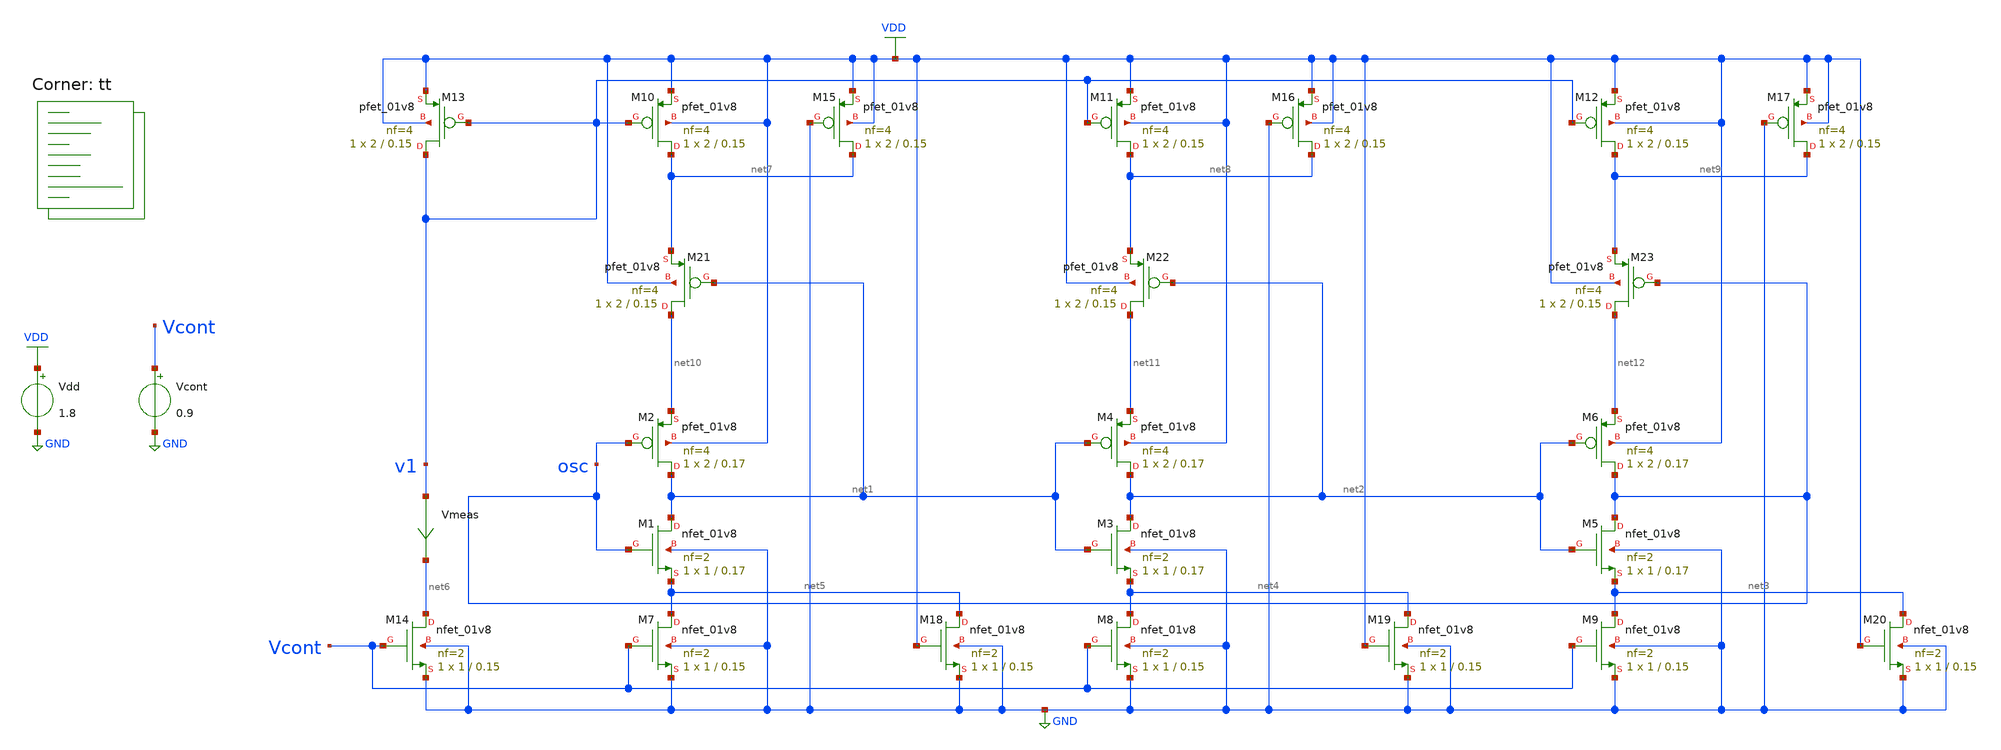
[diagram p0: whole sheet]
** sch_path: projects/pll/vco/xschem_ngspice/tb_current_starved_VCO2.sch
**.subckt tb_current_starved_VCO2
XM1 net1 osc net5 GND sky130_fd_pr__nfet_01v8 L=0.17 W=1 nf=2 ad='int((nf+1)/2) * W/nf * 0.29' as='int((nf+2)/2) * W/nf * 0.29'
+ pd='2*int((nf+1)/2) * (W/nf + 0.29)' ps='2*int((nf+2)/2) * (W/nf + 0.29)' nrd='0.29 / W' nrs='0.29 / W'
+ sa=0 sb=0 sd=0 mult=1 m=1
XM2 net1 osc net10 VDD sky130_fd_pr__pfet_01v8 L=0.17 W=2 nf=4 ad='int((nf+1)/2) * W/nf * 0.29' as='int((nf+2)/2) * W/nf * 0.29'
+ pd='2*int((nf+1)/2) * (W/nf + 0.29)' ps='2*int((nf+2)/2) * (W/nf + 0.29)' nrd='0.29 / W' nrs='0.29 / W'
+ sa=0 sb=0 sd=0 mult=1 m=1
XM3 net2 net1 net4 GND sky130_fd_pr__nfet_01v8 L=0.17 W=1 nf=2 ad='int((nf+1)/2) * W/nf * 0.29' as='int((nf+2)/2) * W/nf * 0.29'
+ pd='2*int((nf+1)/2) * (W/nf + 0.29)' ps='2*int((nf+2)/2) * (W/nf + 0.29)' nrd='0.29 / W' nrs='0.29 / W'
+ sa=0 sb=0 sd=0 mult=1 m=1
XM4 net2 net1 net11 VDD sky130_fd_pr__pfet_01v8 L=0.17 W=2 nf=4 ad='int((nf+1)/2) * W/nf * 0.29' as='int((nf+2)/2) * W/nf * 0.29'
+ pd='2*int((nf+1)/2) * (W/nf + 0.29)' ps='2*int((nf+2)/2) * (W/nf + 0.29)' nrd='0.29 / W' nrs='0.29 / W'
+ sa=0 sb=0 sd=0 mult=1 m=1
XM5 osc net2 net3 GND sky130_fd_pr__nfet_01v8 L=0.17 W=1 nf=2 ad='int((nf+1)/2) * W/nf * 0.29' as='int((nf+2)/2) * W/nf * 0.29'
+ pd='2*int((nf+1)/2) * (W/nf + 0.29)' ps='2*int((nf+2)/2) * (W/nf + 0.29)' nrd='0.29 / W' nrs='0.29 / W'
+ sa=0 sb=0 sd=0 mult=1 m=1
XM6 osc net2 net12 VDD sky130_fd_pr__pfet_01v8 L=0.17 W=2 nf=4 ad='int((nf+1)/2) * W/nf * 0.29' as='int((nf+2)/2) * W/nf * 0.29'
+ pd='2*int((nf+1)/2) * (W/nf + 0.29)' ps='2*int((nf+2)/2) * (W/nf + 0.29)' nrd='0.29 / W' nrs='0.29 / W'
+ sa=0 sb=0 sd=0 mult=1 m=1
XM7 net5 Vcont GND GND sky130_fd_pr__nfet_01v8 L=0.15 W=1 nf=2 ad='int((nf+1)/2) * W/nf * 0.29' as='int((nf+2)/2) * W/nf * 0.29'
+ pd='2*int((nf+1)/2) * (W/nf + 0.29)' ps='2*int((nf+2)/2) * (W/nf + 0.29)' nrd='0.29 / W' nrs='0.29 / W'
+ sa=0 sb=0 sd=0 mult=1 m=1
XM8 net4 Vcont GND GND sky130_fd_pr__nfet_01v8 L=0.15 W=1 nf=2 ad='int((nf+1)/2) * W/nf * 0.29' as='int((nf+2)/2) * W/nf * 0.29'
+ pd='2*int((nf+1)/2) * (W/nf + 0.29)' ps='2*int((nf+2)/2) * (W/nf + 0.29)' nrd='0.29 / W' nrs='0.29 / W'
+ sa=0 sb=0 sd=0 mult=1 m=1
XM9 net3 Vcont GND GND sky130_fd_pr__nfet_01v8 L=0.15 W=1 nf=2 ad='int((nf+1)/2) * W/nf * 0.29' as='int((nf+2)/2) * W/nf * 0.29'
+ pd='2*int((nf+1)/2) * (W/nf + 0.29)' ps='2*int((nf+2)/2) * (W/nf + 0.29)' nrd='0.29 / W' nrs='0.29 / W'
+ sa=0 sb=0 sd=0 mult=1 m=1
XM10 net7 v1 VDD VDD sky130_fd_pr__pfet_01v8 L=0.15 W=2 nf=4 ad='int((nf+1)/2) * W/nf * 0.29' as='int((nf+2)/2) * W/nf * 0.29'
+ pd='2*int((nf+1)/2) * (W/nf + 0.29)' ps='2*int((nf+2)/2) * (W/nf + 0.29)' nrd='0.29 / W' nrs='0.29 / W'
+ sa=0 sb=0 sd=0 mult=1 m=1
XM11 net8 v1 VDD VDD sky130_fd_pr__pfet_01v8 L=0.15 W=2 nf=4 ad='int((nf+1)/2) * W/nf * 0.29' as='int((nf+2)/2) * W/nf * 0.29'
+ pd='2*int((nf+1)/2) * (W/nf + 0.29)' ps='2*int((nf+2)/2) * (W/nf + 0.29)' nrd='0.29 / W' nrs='0.29 / W'
+ sa=0 sb=0 sd=0 mult=1 m=1
XM12 net9 v1 VDD VDD sky130_fd_pr__pfet_01v8 L=0.15 W=2 nf=4 ad='int((nf+1)/2) * W/nf * 0.29' as='int((nf+2)/2) * W/nf * 0.29'
+ pd='2*int((nf+1)/2) * (W/nf + 0.29)' ps='2*int((nf+2)/2) * (W/nf + 0.29)' nrd='0.29 / W' nrs='0.29 / W'
+ sa=0 sb=0 sd=0 mult=1 m=1
Vdd VDD GND 1.8
Vcont Vcont GND 0.9
XM13 v1 v1 VDD VDD sky130_fd_pr__pfet_01v8 L=0.15 W=2 nf=4 ad='int((nf+1)/2) * W/nf * 0.29' as='int((nf+2)/2) * W/nf * 0.29'
+ pd='2*int((nf+1)/2) * (W/nf + 0.29)' ps='2*int((nf+2)/2) * (W/nf + 0.29)' nrd='0.29 / W' nrs='0.29 / W'
+ sa=0 sb=0 sd=0 mult=1 m=1
XM14 net6 Vcont GND GND sky130_fd_pr__nfet_01v8 L=0.15 W=1 nf=2 ad='int((nf+1)/2) * W/nf * 0.29' as='int((nf+2)/2) * W/nf * 0.29'
+ pd='2*int((nf+1)/2) * (W/nf + 0.29)' ps='2*int((nf+2)/2) * (W/nf + 0.29)' nrd='0.29 / W' nrs='0.29 / W'
+ sa=0 sb=0 sd=0 mult=1 m=1
Vmeas v1 net6 0
.save i(vmeas)
XM15 net7 GND VDD VDD sky130_fd_pr__pfet_01v8 L=0.15 W=2 nf=4 ad='int((nf+1)/2) * W/nf * 0.29' as='int((nf+2)/2) * W/nf * 0.29'
+ pd='2*int((nf+1)/2) * (W/nf + 0.29)' ps='2*int((nf+2)/2) * (W/nf + 0.29)' nrd='0.29 / W' nrs='0.29 / W'
+ sa=0 sb=0 sd=0 mult=1 m=1
XM16 net8 GND VDD VDD sky130_fd_pr__pfet_01v8 L=0.15 W=2 nf=4 ad='int((nf+1)/2) * W/nf * 0.29' as='int((nf+2)/2) * W/nf * 0.29'
+ pd='2*int((nf+1)/2) * (W/nf + 0.29)' ps='2*int((nf+2)/2) * (W/nf + 0.29)' nrd='0.29 / W' nrs='0.29 / W'
+ sa=0 sb=0 sd=0 mult=1 m=1
XM17 net9 GND VDD VDD sky130_fd_pr__pfet_01v8 L=0.15 W=2 nf=4 ad='int((nf+1)/2) * W/nf * 0.29' as='int((nf+2)/2) * W/nf * 0.29'
+ pd='2*int((nf+1)/2) * (W/nf + 0.29)' ps='2*int((nf+2)/2) * (W/nf + 0.29)' nrd='0.29 / W' nrs='0.29 / W'
+ sa=0 sb=0 sd=0 mult=1 m=1
XM18 net5 VDD GND GND sky130_fd_pr__nfet_01v8 L=0.15 W=1 nf=2 ad='int((nf+1)/2) * W/nf * 0.29' as='int((nf+2)/2) * W/nf * 0.29'
+ pd='2*int((nf+1)/2) * (W/nf + 0.29)' ps='2*int((nf+2)/2) * (W/nf + 0.29)' nrd='0.29 / W' nrs='0.29 / W'
+ sa=0 sb=0 sd=0 mult=1 m=1
XM19 net4 VDD GND GND sky130_fd_pr__nfet_01v8 L=0.15 W=1 nf=2 ad='int((nf+1)/2) * W/nf * 0.29' as='int((nf+2)/2) * W/nf * 0.29'
+ pd='2*int((nf+1)/2) * (W/nf + 0.29)' ps='2*int((nf+2)/2) * (W/nf + 0.29)' nrd='0.29 / W' nrs='0.29 / W'
+ sa=0 sb=0 sd=0 mult=1 m=1
XM20 net3 VDD GND GND sky130_fd_pr__nfet_01v8 L=0.15 W=1 nf=2 ad='int((nf+1)/2) * W/nf * 0.29' as='int((nf+2)/2) * W/nf * 0.29'
+ pd='2*int((nf+1)/2) * (W/nf + 0.29)' ps='2*int((nf+2)/2) * (W/nf + 0.29)' nrd='0.29 / W' nrs='0.29 / W'
+ sa=0 sb=0 sd=0 mult=1 m=1
XM21 net10 net1 net7 VDD sky130_fd_pr__pfet_01v8 L=0.15 W=2 nf=4 ad='int((nf+1)/2) * W/nf * 0.29' as='int((nf+2)/2) * W/nf * 0.29'
+ pd='2*int((nf+1)/2) * (W/nf + 0.29)' ps='2*int((nf+2)/2) * (W/nf + 0.29)' nrd='0.29 / W' nrs='0.29 / W'
+ sa=0 sb=0 sd=0 mult=1 m=1
XM22 net11 net2 net8 VDD sky130_fd_pr__pfet_01v8 L=0.15 W=2 nf=4 ad='int((nf+1)/2) * W/nf * 0.29' as='int((nf+2)/2) * W/nf * 0.29'
+ pd='2*int((nf+1)/2) * (W/nf + 0.29)' ps='2*int((nf+2)/2) * (W/nf + 0.29)' nrd='0.29 / W' nrs='0.29 / W'
+ sa=0 sb=0 sd=0 mult=1 m=1
XM23 net12 osc net9 VDD sky130_fd_pr__pfet_01v8 L=0.15 W=2 nf=4 ad='int((nf+1)/2) * W/nf * 0.29' as='int((nf+2)/2) * W/nf * 0.29'
+ pd='2*int((nf+1)/2) * (W/nf + 0.29)' ps='2*int((nf+2)/2) * (W/nf + 0.29)' nrd='0.29 / W' nrs='0.29 / W'
+ sa=0 sb=0 sd=0 mult=1 m=1
**** begin user architecture code
.lib $::SKYWATER_MODELS/sky130.lib.spice tt



.option method=gear
.option wnflag=1


.ic v(osc)=0

.temp = 75

Xmeasure osc freq2 measure_Kvco thresh=0.9 dir=1

.control

  pre_osdi ./measure_Kvco.osdi

  let v_cont_start = 0.6
  let v_cont_stop = 1.9

  dowhile v_cont_start <= v_cont_stop
    alter vcont $&v_cont_start
    save v(osc) v(vcont) v(v1) v(v2) v(freq2) i(vmeas) i(vmeas1)
    tran 1ps 30ns
    remzerovec
    write tb_current_starved_VCO2_{$&v_cont_start}.raw
    * linearize v(osc)
    let filename = v_cont_start * 100
    wrdata /foss/designs/my_design/projects/pll/vco/xschem_ngspice/tb_current_starved_VCO2_{$&filename}.txt
+ v(osc)
    set appendwrite

    reset
    let v_cont_start = v_cont_start + 0.1
  end
.endc






**** end user architecture code
**.ends
.GLOBAL VDD
.GLOBAL GND
.end
